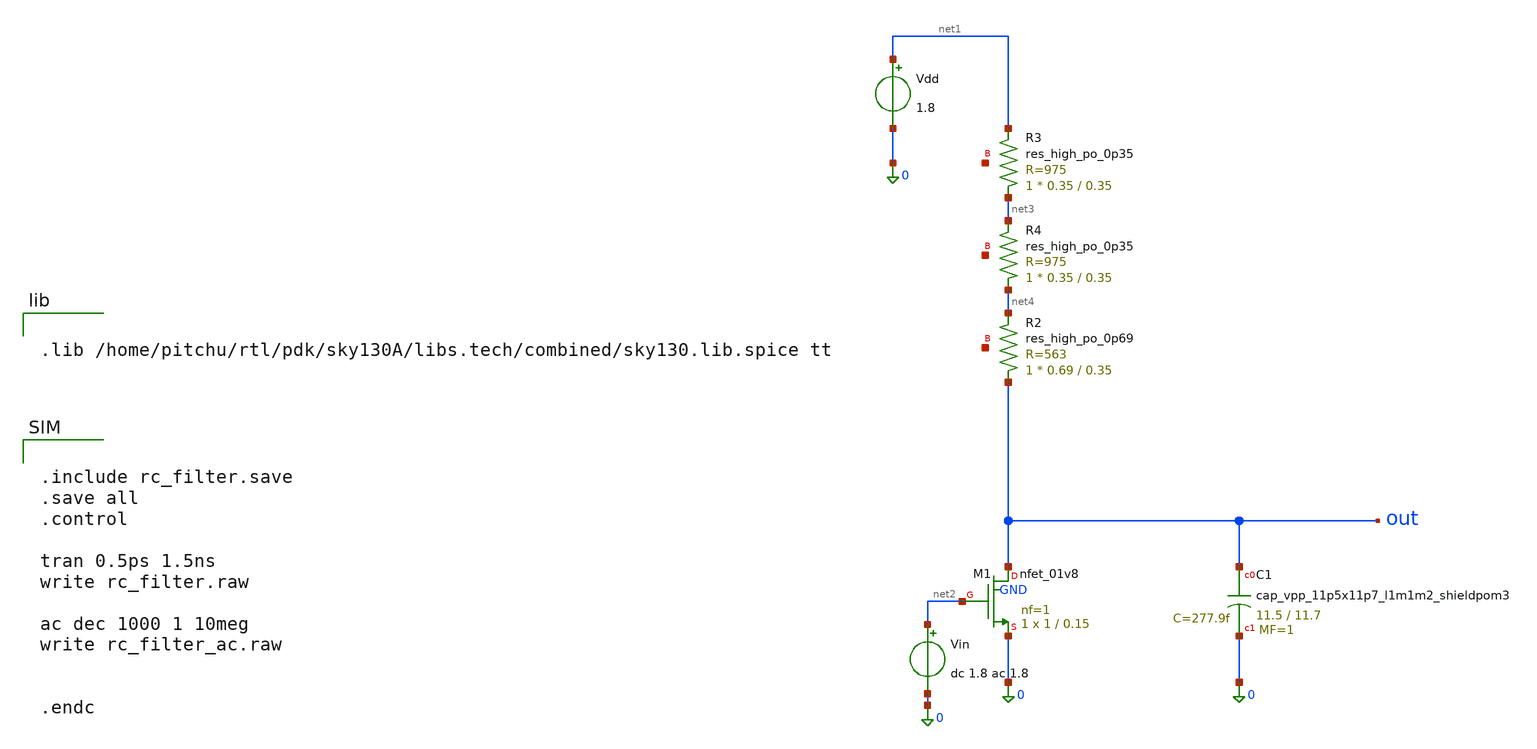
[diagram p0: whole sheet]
** sch_path: experiments/rc_filter.sch
**.subckt rc_filter
XM1 out net2 0 GND sky130_fd_pr__nfet_01v8 L=0.15 W=1 nf=1 ad='int((1 + 1)/2) * 1 / 1 * 0.29' as='int((1 + 2)/2) * 1 / 1 * 0.29'
+ pd='2*int((1 + 1)/2) * (1 / 1 + 0.29)' ps='2*int((1 + 2)/2) * (1 / 1 + 0.29)' nrd='0.29 / 1 ' nrs='0.29 / 1 '
+ sa=0 sb=0 sd=0 mult=1 m=1
Vdd net1 0 1.8
.save i(vdd)
Vin net2 0 dc 1.8 ac 1.8
.save i(vin)
XR3 net3 net1 net5 sky130_fd_pr__res_high_po_0p35 L=0.35 mult=1 m=1
XR4 net4 net3 net6 sky130_fd_pr__res_high_po_0p35 L=0.35 mult=1 m=1
XR2 out net4 net7 sky130_fd_pr__res_high_po_0p69 L=0.35 mult=1 m=1
XC1 out 0 sky130_fd_pr__cap_vpp_11p5x11p7_l1m1m2_shieldpom3 W=11.5 L=11.7 MF=1 m=1
**** begin user architecture code


.lib /home/pitchu/rtl/pdk/sky130A/libs.tech/combined/sky130.lib.spice tt




.include rc_filter.save
.save all
.control

tran 0.5ps 1.5ns
write rc_filter.raw

ac dec 1000 1 10meg
write rc_filter_ac.raw


.endc


**** end user architecture code
**.ends
.end
